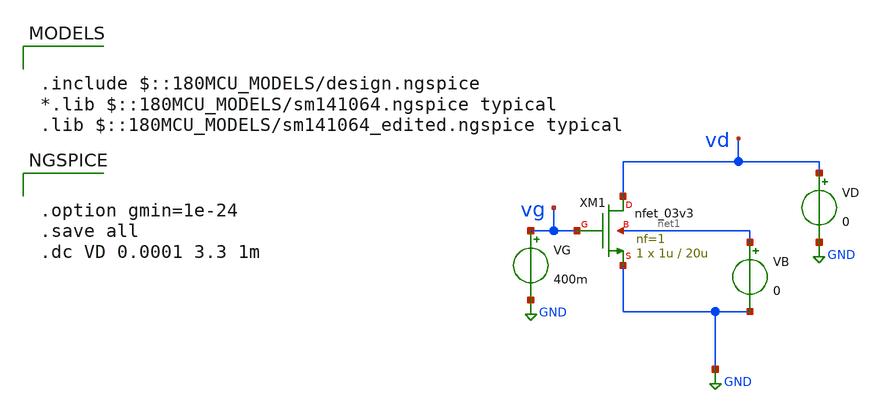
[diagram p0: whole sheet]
** sch_path: gf_tutorials/nmos_IBleak.sch
**.subckt nmos_IBleak
XM1 vd vg GND net1 nfet_03v3 L=20u W=1u nf=1 ad='int((nf+1)/2) * W/nf * 0.18u' as='int((nf+2)/2) * W/nf * 0.18u'
+ pd='2*int((nf+1)/2) * (W/nf + 0.18u)' ps='2*int((nf+2)/2) * (W/nf + 0.18u)' nrd='0.18u / W' nrs='0.18u / W'
+ sa=0 sb=0 sd=0 m=1
VD vd GND 0
VB net1 GND 0
VG vg GND 400m
**** begin user architecture code

.include $::180MCU_MODELS/design.ngspice
*.lib $::180MCU_MODELS/sm141064.ngspice typical
.lib $::180MCU_MODELS/sm141064_edited.ngspice typical



.option gmin=1e-24
.save all
.dc VD 0.0001 3.3 1m


**** end user architecture code
**.ends
.GLOBAL GND
.end
